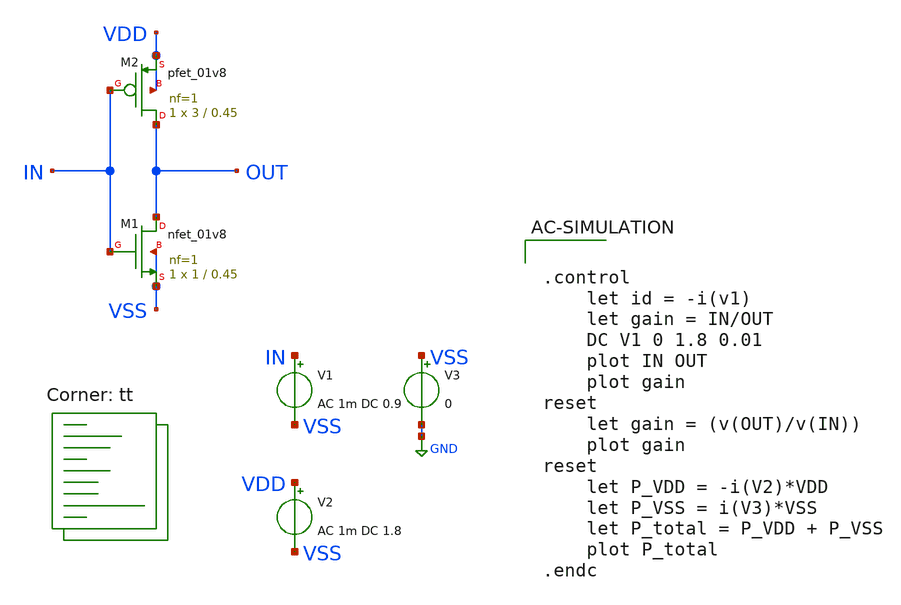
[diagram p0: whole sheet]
** sch_path: designs/libs/core_analog/p-ota/cmos-inverter.sch
**.subckt cmos-inverter
XM1 OUT IN VSS VSS sky130_fd_pr__nfet_01v8 L=0.45 W=1 nf=1 ad='int((nf+1)/2) * W/nf * 0.29' as='int((nf+2)/2) * W/nf * 0.29'
+ pd='2*int((nf+1)/2) * (W/nf + 0.29)' ps='2*int((nf+2)/2) * (W/nf + 0.29)' nrd='0.29 / W' nrs='0.29 / W'
+ sa=0 sb=0 sd=0 mult=1 m=1
XM2 OUT IN VDD VDD sky130_fd_pr__pfet_01v8 L=0.45 W=3 nf=1 ad='int((nf+1)/2) * W/nf * 0.29' as='int((nf+2)/2) * W/nf * 0.29'
+ pd='2*int((nf+1)/2) * (W/nf + 0.29)' ps='2*int((nf+2)/2) * (W/nf + 0.29)' nrd='0.29 / W' nrs='0.29 / W'
+ sa=0 sb=0 sd=0 mult=1 m=1
V1 IN VSS AC 1m DC 0.9
V2 VDD VSS AC 1m DC 1.8
V3 VSS GND 0
**** begin user architecture code
.lib $::SKYWATER_MODELS/sky130.lib.spice tt


.control
	let id = -i(v1)
	let gain = IN/OUT
	DC V1 0 1.8 0.01
	plot IN OUT
	plot gain
reset
	let gain = (v(OUT)/v(IN))
	plot gain
reset
	let P_VDD = -i(V2)*VDD
	let P_VSS = i(V3)*VSS
	let P_total = P_VDD + P_VSS
	plot P_total
.endc

**** end user architecture code
**.ends
.GLOBAL GND
.end
